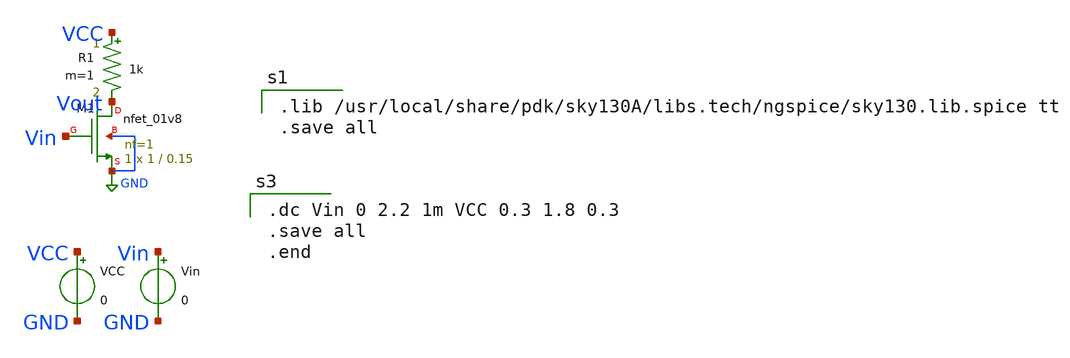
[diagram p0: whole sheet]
** sch_path: Schematic/nmos.sch
**.subckt nmos
VCC VCC GND 0
Vin Vin GND 0
XM1 Vout Vin GND GND sky130_fd_pr__nfet_01v8 L=0.15 W=1 nf=1 ad='int((nf+1)/2) * W/nf * 0.29' as='int((nf+2)/2) * W/nf * 0.29'
+ pd='2*int((nf+1)/2) * (W/nf + 0.29)' ps='2*int((nf+2)/2) * (W/nf + 0.29)' nrd='0.29 / W' nrs='0.29 / W'
+ sa=0 sb=0 sd=0 mult=1 m=1
R1 VCC Vout 1k m=1
**** begin user architecture code

.lib /usr/local/share/pdk/sky130A/libs.tech/ngspice/sky130.lib.spice tt
.save all


.dc Vin 0 2.2 1m VCC 0.3 1.8 0.3
.save all
.end

**** end user architecture code
**.ends
.GLOBAL GND
.end
